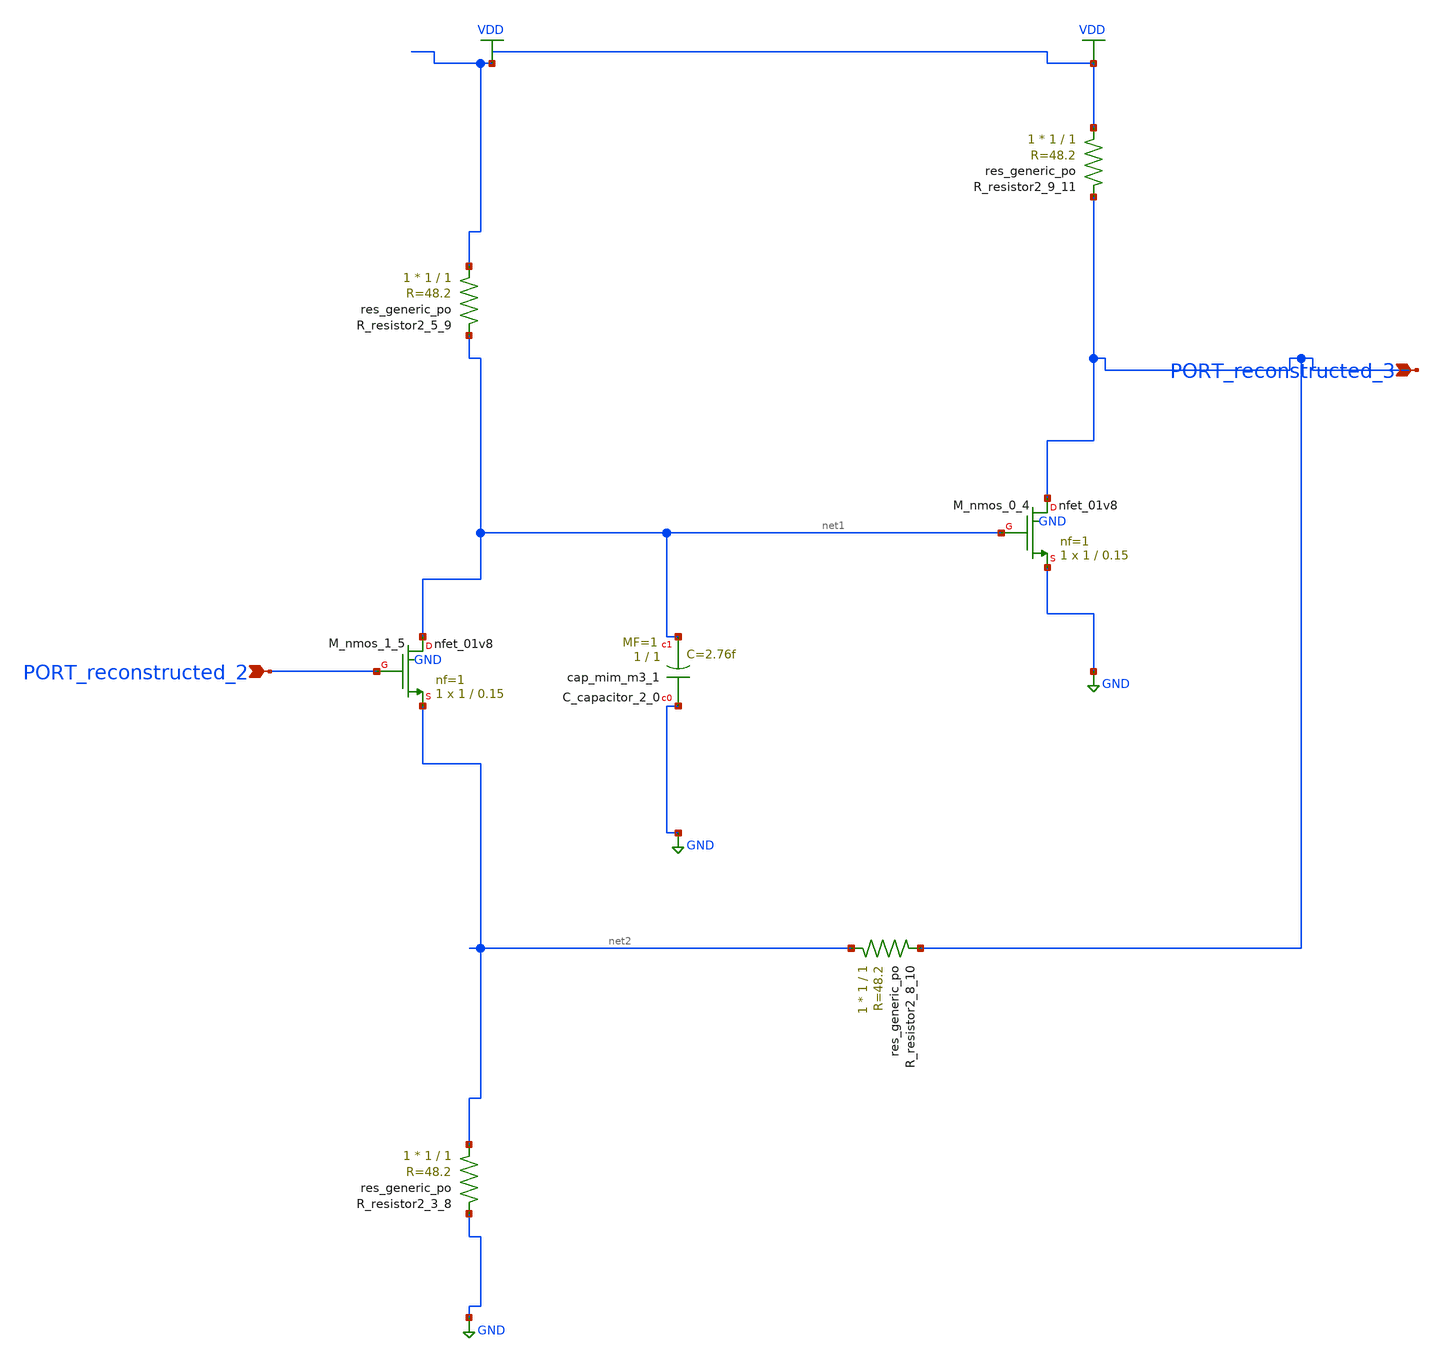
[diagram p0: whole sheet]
** sch_path: schematics/AMSNet/598.sch
**.subckt 598 PORT_reconstructed_2 PORT_reconstructed_3
*.ipin PORT_reconstructed_2
*.ipin PORT_reconstructed_3
XC_capacitor_2_0 GND net1 sky130_fd_pr__cap_mim_m3_1 W=1 L=1 MF=1 m=1
XM_nmos_0_4 PORT_reconstructed_3 net1 GND GND sky130_fd_pr__nfet_01v8 L=0.15 W=1 nf=1 ad='int((1 + 1)/2) * 1 / 1 * 0.29'
+ as='int((1 + 2)/2) * 1 / 1 * 0.29' pd='2*int((1 + 1)/2) * (1 / 1 + 0.29)' ps='2*int((1 + 2)/2) * (1 / 1 + 0.29)'
+ nrd='0.29 / 1 ' nrs='0.29 / 1 ' sa=0 sb=0 sd=0 mult=1 m=1
XM_nmos_1_5 net1 PORT_reconstructed_2 net2 GND sky130_fd_pr__nfet_01v8 L=0.15 W=1 nf=1 ad='int((1 + 1)/2) * 1 / 1 * 0.29'
+ as='int((1 + 2)/2) * 1 / 1 * 0.29' pd='2*int((1 + 1)/2) * (1 / 1 + 0.29)' ps='2*int((1 + 2)/2) * (1 / 1 + 0.29)'
+ nrd='0.29 / 1 ' nrs='0.29 / 1 ' sa=0 sb=0 sd=0 mult=1 m=1
XR_resistor2_3_8 net2 GND sky130_fd_pr__res_generic_po W=1 L=1 m=1
XR_resistor2_5_9 VDD net1 sky130_fd_pr__res_generic_po W=1 L=1 m=1
XR_resistor2_8_10 net2 PORT_reconstructed_3 sky130_fd_pr__res_generic_po W=1 L=1 m=1
XR_resistor2_9_11 VDD PORT_reconstructed_3 sky130_fd_pr__res_generic_po W=1 L=1 m=1
**.ends
.GLOBAL GND
.GLOBAL VDD
.end
